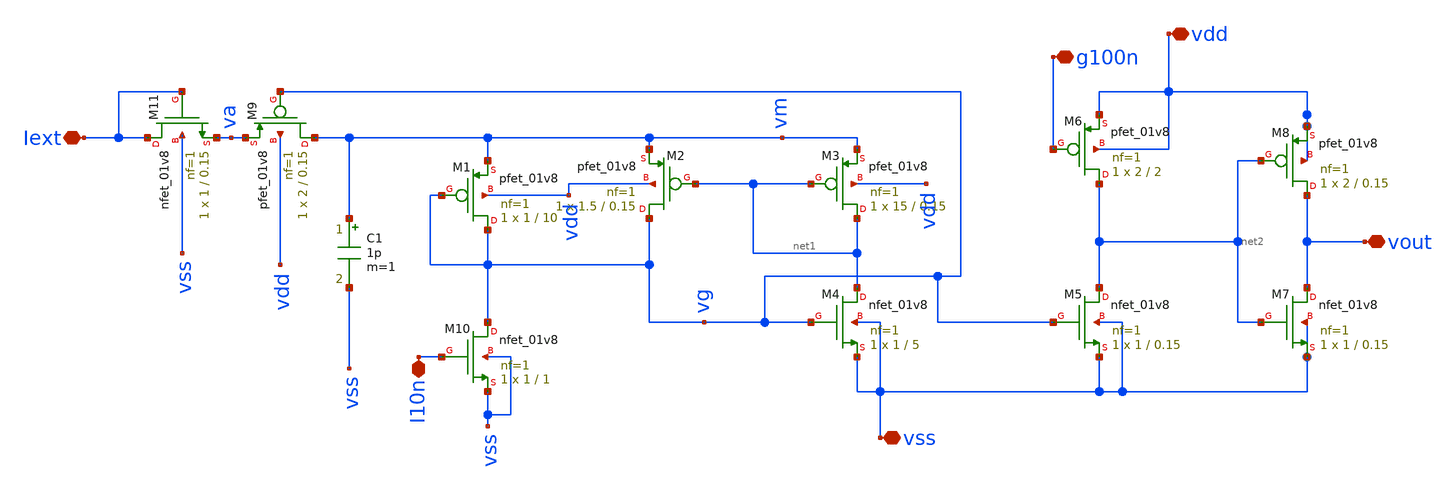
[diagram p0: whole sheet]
** sch_path: Neuron/ultralif/ultralif.sch
**.subckt ultralif Iext vout vss I10n vdd g100n
*.iopin Iext
*.iopin vout
*.iopin vss
*.iopin I10n
*.iopin vdd
*.iopin g100n
XM1 vg vg vm vdd sky130_fd_pr__pfet_01v8 L=10 W=1 nf=1 ad='int((nf+1)/2) * W/nf * 0.29' as='int((nf+2)/2) * W/nf * 0.29'
+ pd='2*int((nf+1)/2) * (W/nf + 0.29)' ps='2*int((nf+2)/2) * (W/nf + 0.29)' nrd='0.29 / W' nrs='0.29 / W'
+ sa=0 sb=0 sd=0 mult=1 m=1
XM2 vg net1 vm vdd sky130_fd_pr__pfet_01v8 L=0.15 W=1.5 nf=1 ad='int((nf+1)/2) * W/nf * 0.29' as='int((nf+2)/2) * W/nf * 0.29'
+ pd='2*int((nf+1)/2) * (W/nf + 0.29)' ps='2*int((nf+2)/2) * (W/nf + 0.29)' nrd='0.29 / W' nrs='0.29 / W'
+ sa=0 sb=0 sd=0 mult=1 m=1
XM3 net1 net1 vm vdd sky130_fd_pr__pfet_01v8 L=0.15 W=15 nf=1 ad='int((nf+1)/2) * W/nf * 0.29' as='int((nf+2)/2) * W/nf * 0.29'
+ pd='2*int((nf+1)/2) * (W/nf + 0.29)' ps='2*int((nf+2)/2) * (W/nf + 0.29)' nrd='0.29 / W' nrs='0.29 / W'
+ sa=0 sb=0 sd=0 mult=1 m=1
XM4 net1 vg vss vss sky130_fd_pr__nfet_01v8 L=5 W=1 nf=1 ad='int((1 + 1)/2) * 1 / 1 * 0.29' as='int((1 + 2)/2) * 1 / 1 * 0.29'
+ pd='2*int((1 + 1)/2) * (1 / 1 + 0.29)' ps='2*int((1 + 2)/2) * (1 / 1 + 0.29)' nrd='0.29 / 1 ' nrs='0.29 / 1 '
+ sa=0 sb=0 sd=0 mult=1 m=1
C1 vm vss 1p m=1
XM10 vg I10n vss vss sky130_fd_pr__nfet_01v8 L=1 W=1 nf=1 ad='int((1 + 1)/2) * 1 / 1 * 0.29' as='int((1 + 2)/2) * 1 / 1 * 0.29'
+ pd='2*int((1 + 1)/2) * (1 / 1 + 0.29)' ps='2*int((1 + 2)/2) * (1 / 1 + 0.29)' nrd='0.29 / 1 ' nrs='0.29 / 1 '
+ sa=0 sb=0 sd=0 mult=1 m=1
XM5 net2 vg vss vss sky130_fd_pr__nfet_01v8 L=0.15 W=1 nf=1 ad='int((1 + 1)/2) * 1 / 1 * 0.29' as='int((1 + 2)/2) * 1 / 1 * 0.29'
+ pd='2*int((1 + 1)/2) * (1 / 1 + 0.29)' ps='2*int((1 + 2)/2) * (1 / 1 + 0.29)' nrd='0.29 / 1 ' nrs='0.29 / 1 '
+ sa=0 sb=0 sd=0 mult=1 m=1
XM6 net2 g100n vdd vdd sky130_fd_pr__pfet_01v8 L=2 W=2 nf=1 ad='int((nf+1)/2) * W/nf * 0.29' as='int((nf+2)/2) * W/nf * 0.29'
+ pd='2*int((nf+1)/2) * (W/nf + 0.29)' ps='2*int((nf+2)/2) * (W/nf + 0.29)' nrd='0.29 / W' nrs='0.29 / W'
+ sa=0 sb=0 sd=0 mult=1 m=1
XM7 vout net2 vss vss sky130_fd_pr__nfet_01v8 L=0.15 W=1 nf=1 ad='int((1 + 1)/2) * 1 / 1 * 0.29' as='int((1 + 2)/2) * 1 / 1 * 0.29'
+ pd='2*int((1 + 1)/2) * (1 / 1 + 0.29)' ps='2*int((1 + 2)/2) * (1 / 1 + 0.29)' nrd='0.29 / 1 ' nrs='0.29 / 1 '
+ sa=0 sb=0 sd=0 mult=1 m=1
XM8 vout net2 vdd vdd sky130_fd_pr__pfet_01v8 L=0.15 W=2 nf=1 ad='int((nf+1)/2) * W/nf * 0.29' as='int((nf+2)/2) * W/nf * 0.29'
+ pd='2*int((nf+1)/2) * (W/nf + 0.29)' ps='2*int((nf+2)/2) * (W/nf + 0.29)' nrd='0.29 / W' nrs='0.29 / W'
+ sa=0 sb=0 sd=0 mult=1 m=1
XM9 vm vg va vdd sky130_fd_pr__pfet_01v8 L=0.15 W=2 nf=1 ad='int((nf+1)/2) * W/nf * 0.29' as='int((nf+2)/2) * W/nf * 0.29'
+ pd='2*int((nf+1)/2) * (W/nf + 0.29)' ps='2*int((nf+2)/2) * (W/nf + 0.29)' nrd='0.29 / W' nrs='0.29 / W'
+ sa=0 sb=0 sd=0 mult=1 m=1
XM11 Iext Iext va vss sky130_fd_pr__nfet_01v8 L=0.15 W=1 nf=1 ad='int((1 + 1)/2) * 1 / 1 * 0.29' as='int((1 + 2)/2) * 1 / 1 * 0.29'
+ pd='2*int((1 + 1)/2) * (1 / 1 + 0.29)' ps='2*int((1 + 2)/2) * (1 / 1 + 0.29)' nrd='0.29 / 1 ' nrs='0.29 / 1 '
+ sa=0 sb=0 sd=0 mult=1 m=1
**.ends
.end
